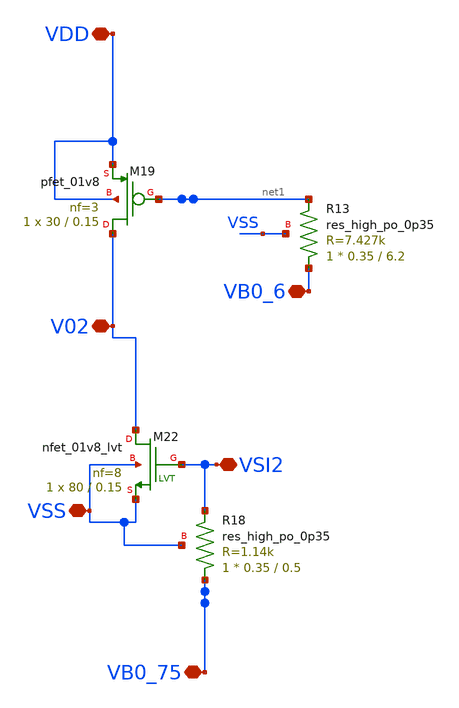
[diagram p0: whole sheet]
** sch_path: xschem/xschem4_sic_oct_20/partition4.sch
**.subckt partition4 VSI2 VB0_6 VDD VSS VB0_75 V02
*.iopin VSI2
*.iopin VB0_6
*.iopin VDD
*.iopin VSS
*.iopin VB0_75
*.iopin V02
XM19 V02 net1 VDD VDD sky130_fd_pr__pfet_01v8 L=0.15 W=30 nf=3 ad='int((nf+1)/2) * W/nf * 0.29' as='int((nf+2)/2) * W/nf * 0.29'
+ pd='2*int((nf+1)/2) * (W/nf + 0.29)' ps='2*int((nf+2)/2) * (W/nf + 0.29)' nrd='0.29 / W' nrs='0.29 / W'
+ sa=0 sb=0 sd=0 mult=1 m=1
XR13 VB0_6 net1 VSS sky130_fd_pr__res_high_po_0p35 L=6.2 mult=1 m=1
XM22 V02 VSI2 VSS VSS sky130_fd_pr__nfet_01v8_lvt L=0.15 W=80 nf=8 ad='int((nf+1)/2) * W/nf * 0.29' as='int((nf+2)/2) * W/nf * 0.29'
+ pd='2*int((nf+1)/2) * (W/nf + 0.29)' ps='2*int((nf+2)/2) * (W/nf + 0.29)' nrd='0.29 / W' nrs='0.29 / W'
+ sa=0 sb=0 sd=0 mult=1 m=1
XR18 VB0_75 VSI2 VSS sky130_fd_pr__res_high_po_0p35 L=0.5 mult=1 m=1
**.ends
.end
